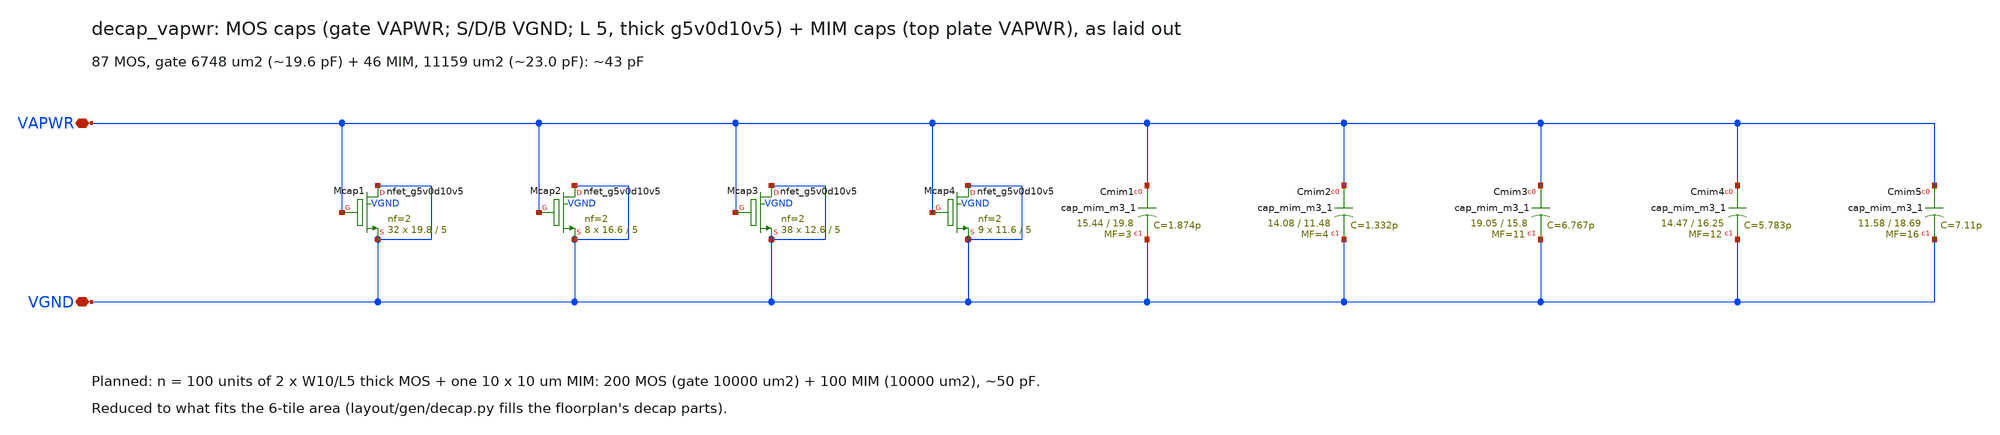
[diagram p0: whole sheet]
** sch_path: xschem/decap_vapwr.sch
**.subckt decap_vapwr VAPWR VGND
*.iopin VAPWR
*.iopin VGND
XMcap1 VGND VAPWR VGND VGND sky130_fd_pr__nfet_g5v0d10v5 L=5 W=19.8 nf=2 ad='int((nf+1)/2) * W/nf * 0.29'
+ as='int((nf+2)/2) * W/nf * 0.29' pd='2*int((nf+1)/2) * (W/nf + 0.29)' ps='2*int((nf+2)/2) * (W/nf + 0.29)'
+ nrd='0.29 / W' nrs='0.29 / W' sa=0 sb=0 sd=0 mult=32 m=32
XMcap2 VGND VAPWR VGND VGND sky130_fd_pr__nfet_g5v0d10v5 L=5 W=16.6 nf=2 ad='int((nf+1)/2) * W/nf * 0.29'
+ as='int((nf+2)/2) * W/nf * 0.29' pd='2*int((nf+1)/2) * (W/nf + 0.29)' ps='2*int((nf+2)/2) * (W/nf + 0.29)'
+ nrd='0.29 / W' nrs='0.29 / W' sa=0 sb=0 sd=0 mult=8 m=8
XMcap3 VGND VAPWR VGND VGND sky130_fd_pr__nfet_g5v0d10v5 L=5 W=12.6 nf=2 ad='int((nf+1)/2) * W/nf * 0.29'
+ as='int((nf+2)/2) * W/nf * 0.29' pd='2*int((nf+1)/2) * (W/nf + 0.29)' ps='2*int((nf+2)/2) * (W/nf + 0.29)'
+ nrd='0.29 / W' nrs='0.29 / W' sa=0 sb=0 sd=0 mult=38 m=38
XMcap4 VGND VAPWR VGND VGND sky130_fd_pr__nfet_g5v0d10v5 L=5 W=11.6 nf=2 ad='int((nf+1)/2) * W/nf * 0.29'
+ as='int((nf+2)/2) * W/nf * 0.29' pd='2*int((nf+1)/2) * (W/nf + 0.29)' ps='2*int((nf+2)/2) * (W/nf + 0.29)'
+ nrd='0.29 / W' nrs='0.29 / W' sa=0 sb=0 sd=0 mult=9 m=9
XCmim1 VAPWR VGND sky130_fd_pr__cap_mim_m3_1 W=15.44 L=19.8 MF=3 m=3
XCmim2 VAPWR VGND sky130_fd_pr__cap_mim_m3_1 W=14.08 L=11.48 MF=4 m=4
XCmim3 VAPWR VGND sky130_fd_pr__cap_mim_m3_1 W=19.05 L=15.8 MF=11 m=11
XCmim4 VAPWR VGND sky130_fd_pr__cap_mim_m3_1 W=14.47 L=16.25 MF=12 m=12
XCmim5 VAPWR VGND sky130_fd_pr__cap_mim_m3_1 W=11.58 L=18.69 MF=16 m=16
**.ends
.end
